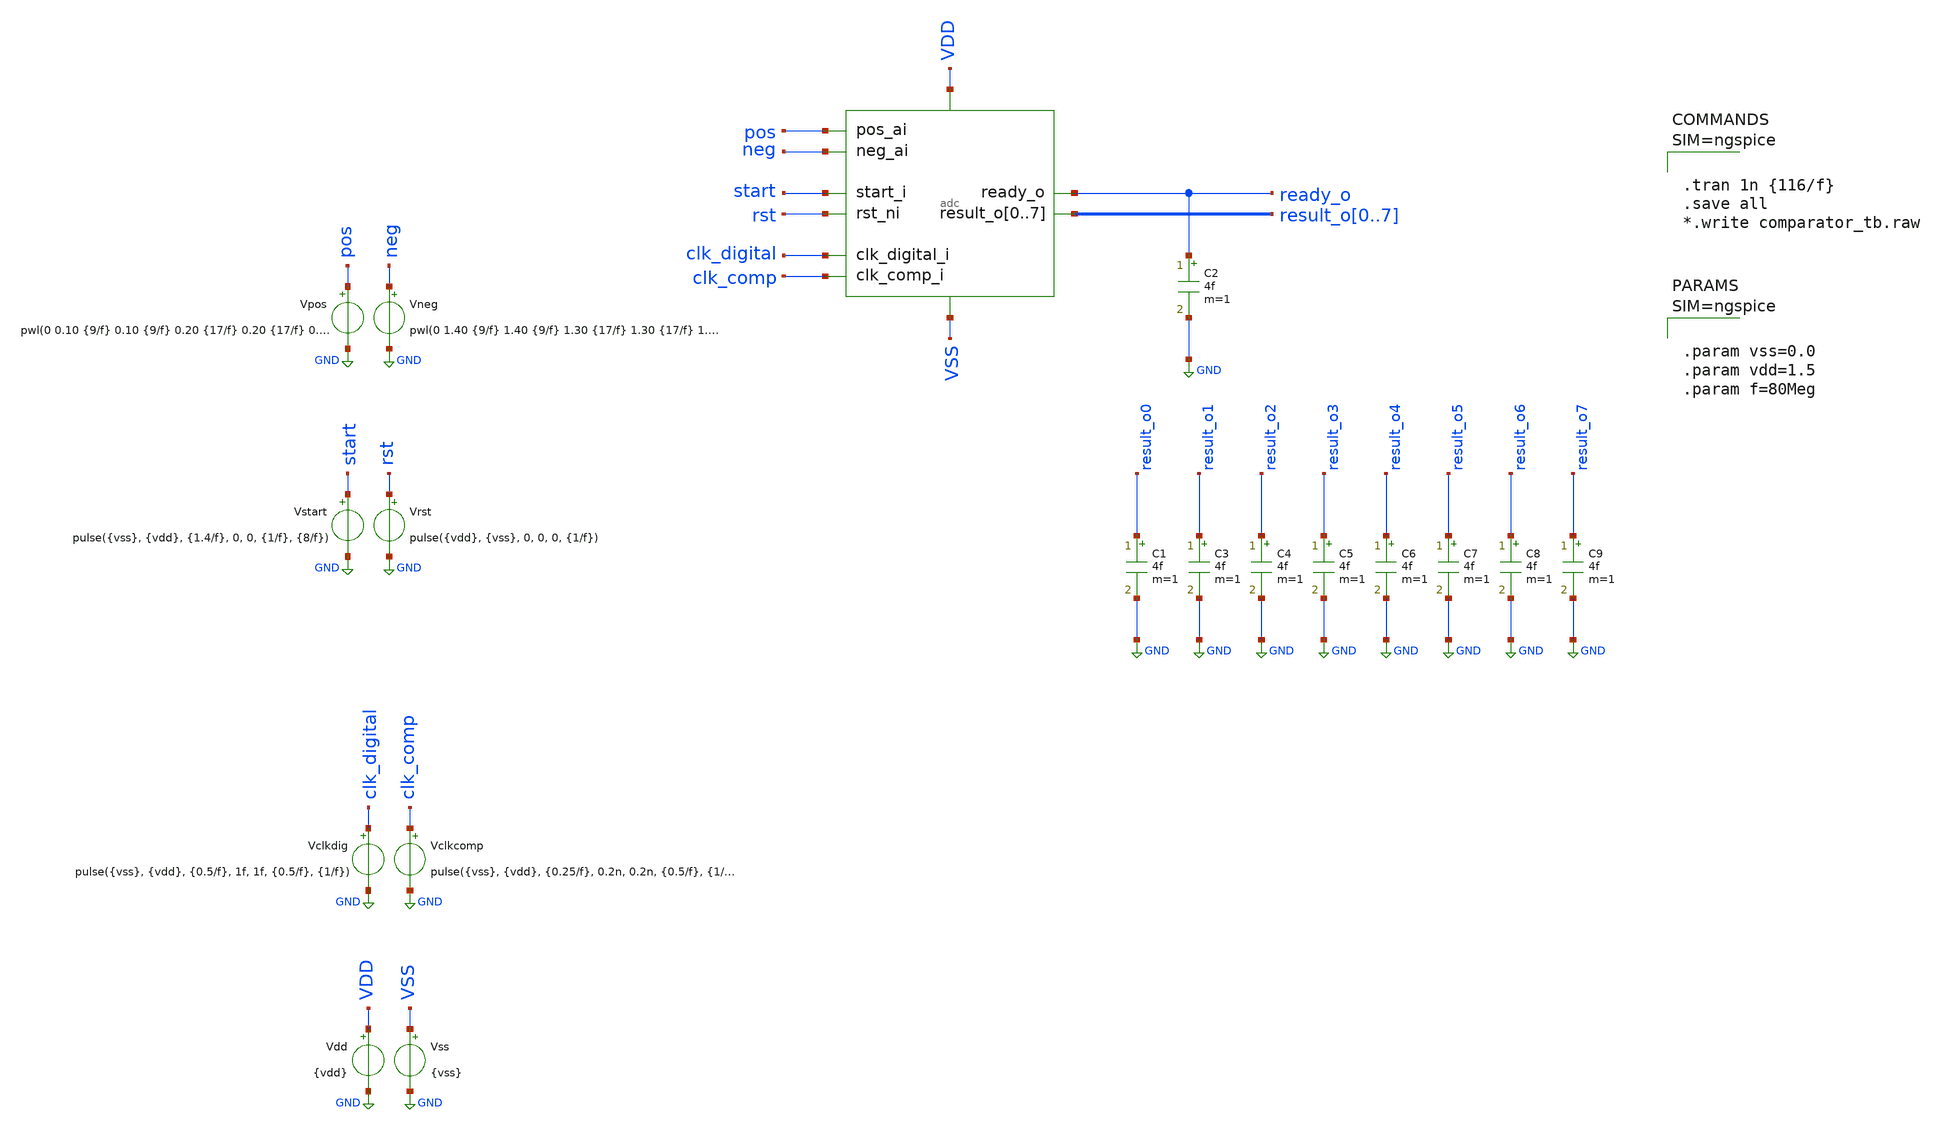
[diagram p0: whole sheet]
** sch_path: designs/diff/xschem/adc_tb.sch
* IHP-GmbH/IHP-Open-PDK/ihp-sg13g2/libs.tech/xschem/sg13g2_stdcells/sg13g2_inv_2.sch:
* Copyright 2023 IHP PDK Authors
* Licensed under the Apache License, Version 2.0 (the "License");
**.subckt adc_tb
x1 pos start rst clk_digital result_o0 result_o1 result_o2 result_o3 result_o4 result_o5 result_o6
+ result_o7 ready_o VDD VSS clk_comp neg adc
Vclkdig clk_digital GND pulse({vss}, {vdd}, {0.5/f}, 1f, 1f, {0.5/f}, {1/f})
Vrst rst GND pulse({vdd}, {vss}, 0, 0, 0, {1/f})
Vstart start GND pulse({vss}, {vdd}, {1.4/f}, 0, 0, {1/f}, {8/f})
Vpos pos GND pwl(0 0.10 {9/f} 0.10 {9/f} 0.20 {17/f} 0.20 {17/f} 0.30 {25/f} 0.30 {25/f} 0.40 {33/f}
+ 0.40 {33/f} 0.50 {41/f} 0.50 {41/f} 0.60 {49/f} 0.60 {49/f} 0.70 {57/f} 0.70 {57/f} 0.80 {65/f} 0.80
+ {65/f} 0.90 {73/f} 0.90 {73/f} 1.00 {81/f} 1.00 {81/f} 1.10 {89/f} 1.10 {89/f} 1.20 {97/f} 1.20 {97/f}
+ 1.30 {105/f} 1.30 {105/f} 1.40 {113/f} 1.40)
.save i(vpos)
Vdd VDD GND {vdd}
Vss VSS GND {vss}
C1 result_o0 GND 4f m=1
C2 ready_o GND 4f m=1
C3 result_o1 GND 4f m=1
C4 result_o2 GND 4f m=1
C5 result_o3 GND 4f m=1
Vclkcomp clk_comp GND pulse({vss}, {vdd}, {0.25/f}, 0.2n, 0.2n, {0.5/f}, {1/f})
C6 result_o4 GND 4f m=1
C7 result_o5 GND 4f m=1
C8 result_o6 GND 4f m=1
C9 result_o7 GND 4f m=1
Vneg neg GND pwl(0 1.40 {9/f} 1.40 {9/f} 1.30 {17/f} 1.30 {17/f} 1.20 {25/f} 1.20 {25/f} 1.10 {33/f}
+ 1.10 {33/f} 1.00 {41/f} 1.00 {41/f} 0.90 {49/f} 0.90 {49/f} 0.80 {57/f} 0.80 {57/f} 0.70 {65/f} 0.70
+ {65/f} 0.60 {73/f} 0.60 {73/f} 0.50 {81/f} 0.50 {81/f} 0.40 {89/f} 0.40 {89/f} 0.30 {97/f} 0.30 {97/f}
+ 0.20 {105/f} 0.20 {105/f} 0.10 {113/f} 0.10)
.save i(vneg)
**** begin user architecture code

.lib $::SG13G2_MODELS/cornerMOSlv.lib mos_tt
.lib $::SG13G2_MODELS/cornerCAP.lib cap_typ
.include $::PDK_ROOT/ihp-sg13g2/libs.ref/sg13g2_stdcell/spice/sg13g2_stdcell.spice




.tran 1n {116/f}
.save all
*.write comparator_tb.raw






.param vss=0.0
.param vdd=1.5
.param f=80Meg






.control
pre_set auto_bridge_d_out =  ( ".model auto_bridge_out bidi_bridge(direction=0 out_high=1.5
+ t_rise=0.2n t_fall=0.2n)"    "auto_bridge_out%d [ %s ] [ %s ] null auto_bridge_out" )
pre_set auto_bridge_d_in =  ( ".model auto_bridge_in bidi_bridge(direction=1 in_low=0.5 in_high=1)"
+    "auto_bridge_in%d [ %s ] [ %s ] null auto_bridge_in" )
.endc



**** end user architecture code
**.ends

* expanding   symbol:  adc.sym # of pins=10
** sym_path: designs/diff/xschem/adc.sym
** sch_path: designs/diff/xschem/adc.sch
.subckt adc pos_ai start_i rst_ni clk_digital_i result_o0 result_o1 result_o2 result_o3 result_o4
+ result_o5 result_o6 result_o7 ready_o VDD VSS clk_comp_i neg_ai
*.ipin pos_ai
*.ipin clk_digital_i
*.ipin VSS
*.ipin VDD
*.ipin rst_ni
*.ipin start_i
*.opin ready_o
*.opin result_o0,result_o1,result_o2,result_o3,result_o4,result_o5,result_o6,result_o7
*.ipin clk_comp_i
*.ipin neg_ai
A2 [ clk_digital_i ] [ net1 ] adc_buff_clk
A1 [ net1 start_i rst_ni comp_p comp_n ] [ sample dac_p0 dac_p1 dac_p2 dac_p3 dac_p4 dac_p5 dac_p6
+ dac_p7 dac_n0 dac_n1 dac_n2 dac_n3 dac_n4 dac_n5 dac_n6 dac_n7 ready_o result_o0 result_o1 result_o2
+ result_o3 result_o4 result_o5 result_o6 result_o7 ] adc
A3 [ %vd(pos neg) ] [ comp ] comp
A4 [ comp ] [ comp_a ] dac_buff
* noconn %vd(pos neg)
x2 net2 pos neg comp_2 comp_1 VSS VDD net3 comparator
x4 pos neg VSS VDD dac_p0 dac_p1 dac_p2 dac_p3 dac_p4 dac_p5 dac_p6 dac_p7 dac_n0 dac_n1 dac_n2
+ dac_n3 dac_n4 dac_n5 dac_n6 dac_n7 cdac
* noconn comp_a
XM5 comp_p comp_1 VSS VSS sg13_lv_nmos w=1.5u l=0.13u ng=1 m=1 mm_ok=1
XM6 comp_p comp_1 VDD VDD sg13_lv_pmos w=0.15u l=0.13u ng=1 m=1 mm_ok=1
XM7 comp_n comp_2 VSS VSS sg13_lv_nmos w=1.5u l=0.13u ng=1 m=1 mm_ok=1
XM8 comp_n comp_2 VDD VDD sg13_lv_pmos w=0.15u l=0.13u ng=1 m=1 mm_ok=1
.ends


* expanding   symbol:  ../../comparator/comparator.sym # of pins=8
** sym_path: designs/comparator_dt/comparator.sym
** sch_path: designs/comparator_dt/comparator.sch
.subckt comparator clk_i pos_ai neg_ai neg_o pos_o VSS VDD clk_ni
*.ipin pos_ai
*.ipin neg_ai
*.ipin VSS
*.ipin VDD
*.opin neg_o
*.opin pos_o
*.ipin clk_i
*.ipin clk_ni
XM12 neg_buf clk_i VDD VDD sg13_lv_pmos w=1.0u l=0.13u ng=1 m=1 mm_ok=1
XM13 pos_buf clk_i VDD VDD sg13_lv_pmos w=1.0u l=0.13u ng=1 m=1 mm_ok=1
XM14 net1 pos_ai neg_buf VSS sg13_lv_nmos w=1.0u l=0.13u ng=1 m=1 mm_ok=1
XM15 net1 neg_ai pos_buf VSS sg13_lv_nmos w=1.0u l=0.13u ng=1 m=1 mm_ok=1
XM16 VSS clk_i net1 VSS sg13_lv_nmos w=1.0u l=0.13u ng=1 m=1 mm_ok=1
XM17 net2 clk_ni VDD VDD sg13_lv_pmos w=2.0u l=0.13u ng=2 m=1 mm_ok=1
XM18 pos_o neg_o net2 VDD sg13_lv_pmos w=2.0u l=0.13u ng=2 m=1 mm_ok=1
XM19 neg_o pos_o net2 VDD sg13_lv_pmos w=2.0u l=0.13u ng=2 m=1 mm_ok=1
XM20 VSS neg_buf pos_o VSS sg13_lv_nmos w=1.0u l=0.13u ng=1 m=1 mm_ok=1
XM21 VSS neg_o pos_o VSS sg13_lv_nmos w=1.0u l=0.13u ng=1 m=1 mm_ok=1
XM22 VSS pos_o neg_o VSS sg13_lv_nmos w=1.0u l=0.13u ng=1 m=1 mm_ok=1
XM23 VSS pos_buf neg_o VSS sg13_lv_nmos w=1.0u l=0.13u ng=1 m=1 mm_ok=1
XC1 neg_buf VSS cap_cmim w=1.41e-5 l=1.41e-5 m=1 mm_ok=1
XC2 pos_buf VSS cap_cmim w=1.41e-5 l=1.41e-5 m=1 mm_ok=1
.ends


* expanding   symbol:  ../../cdac_diff/cdac.sym # of pins=6
** sym_path: designs/cdac_diff/cdac.sym
** sch_path: designs/cdac_diff/cdac.sch
.subckt cdac pos_ai neg_ai VSS VDD pos_ctrl_i0 pos_ctrl_i1 pos_ctrl_i2 pos_ctrl_i3 pos_ctrl_i4
+ pos_ctrl_i5 pos_ctrl_i6 pos_ctrl_i7 neg_ctrl_i0 neg_ctrl_i1 neg_ctrl_i2 neg_ctrl_i3 neg_ctrl_i4 neg_ctrl_i5
+ neg_ctrl_i6 neg_ctrl_i7
*.ipin pos_ai
*.ipin VSS
*.ipin VDD
*.ipin neg_ai
*.ipin
*+ pos_ctrl_i0,pos_ctrl_i1,pos_ctrl_i2,pos_ctrl_i3,pos_ctrl_i4,pos_ctrl_i5,pos_ctrl_i6,pos_ctrl_i7
*.ipin
*+ neg_ctrl_i0,neg_ctrl_i1,neg_ctrl_i2,neg_ctrl_i3,neg_ctrl_i4,neg_ctrl_i5,neg_ctrl_i6,neg_ctrl_i7
x1 net1 pos_ctrl_i0 VDD VSS sg13g2_inv_2
x2 net2 pos_ctrl_i1 VDD VSS sg13g2_inv_2
x3 net3 pos_ctrl_i2 VDD VSS sg13g2_inv_2
x4 net4 pos_ctrl_i3 VDD VSS sg13g2_inv_2
x5 net5 pos_ctrl_i4 VDD VSS sg13g2_inv_2
x6 net6 pos_ctrl_i5 VDD VSS sg13g2_inv_2
x7 net7 pos_ctrl_i6 VDD VSS sg13g2_inv_2
x8 net8 pos_ctrl_i7 VDD VSS sg13g2_inv_2
XC1 pos_ai net8 cap_cmim w=2.5292e-6 l=2.5292e-6 m=1 mm_ok=1
XC2 pos_ai net7 cap_cmim w=2.5292e-6 l=2.5292e-6 m=2 mm_ok=1
XC3 pos_ai net6 cap_cmim w=2.5292e-6 l=2.5292e-6 m=4 mm_ok=1
XC4 pos_ai net5 cap_cmim w=2.5292e-6 l=2.5292e-6 m=8 mm_ok=1
XC9 pos_ai VSS cap_cmim w=2.5292e-6 l=2.5292e-6 m=1 mm_ok=1
x9 net9 neg_ctrl_i0 VDD VSS sg13g2_inv_2
x10 net10 neg_ctrl_i1 VDD VSS sg13g2_inv_2
x11 net11 neg_ctrl_i2 VDD VSS sg13g2_inv_2
x12 net12 neg_ctrl_i3 VDD VSS sg13g2_inv_2
x13 net13 neg_ctrl_i4 VDD VSS sg13g2_inv_2
x14 net14 neg_ctrl_i5 VDD VSS sg13g2_inv_2
x15 net15 neg_ctrl_i6 VDD VSS sg13g2_inv_2
x16 net16 neg_ctrl_i7 VDD VSS sg13g2_inv_2
XC10 neg_ai net16 cap_cmim w=2.5292e-6 l=2.5292e-6 m=1 mm_ok=1
XC11 neg_ai net15 cap_cmim w=2.5292e-6 l=2.5292e-6 m=2 mm_ok=1
XC12 neg_ai net14 cap_cmim w=2.5292e-6 l=2.5292e-6 m=4 mm_ok=1
XC13 neg_ai net13 cap_cmim w=2.5292e-6 l=2.5292e-6 m=8 mm_ok=1
XC18 neg_ai VSS cap_cmim w=2.5292e-6 l=2.5292e-6 m=1 mm_ok=1
XC8 pos_ai net1 cap_cmim w=2.5292e-6 l=2.5292e-6 m=64 mm_ok=1
XC17 neg_ai net9 cap_cmim w=2.5292e-6 l=2.5292e-6 m=64 mm_ok=1
XC19 neg_ai net18 cap_cmim w=2.5292e-6 l=2.5292e-6 m=64 mm_ok=1
XC20 pos_ai net17 cap_cmim w=2.5292e-6 l=2.5292e-6 m=64 mm_ok=1
XC7 neg_ai net10 cap_cmim w=2.5292e-6 l=2.5292e-6 m=32 mm_ok=1
XC16 pos_ai net2 cap_cmim w=2.5292e-6 l=2.5292e-6 m=32 mm_ok=1
XC21 pos_ai net19 cap_cmim w=2.5292e-6 l=2.5292e-6 m=32 mm_ok=1
XC22 neg_ai net20 cap_cmim w=2.5292e-6 l=2.5292e-6 m=32 mm_ok=1
XC23 neg_ai net22 cap_cmim w=2.5292e-6 l=2.5292e-6 m=16 mm_ok=1
XC24 pos_ai net21 cap_cmim w=2.5292e-6 l=2.5292e-6 m=16 mm_ok=1
XC6 neg_ai net11 cap_cmim w=2.5292e-6 l=2.5292e-6 m=16 mm_ok=1
XC15 pos_ai net3 cap_cmim w=2.5292e-6 l=2.5292e-6 m=16 mm_ok=1
XC25 neg_ai net24 cap_cmim w=2.5292e-6 l=2.5292e-6 m=8 mm_ok=1
XC26 pos_ai net23 cap_cmim w=2.5292e-6 l=2.5292e-6 m=8 mm_ok=1
XC5 pos_ai net4 cap_cmim w=2.5292e-6 l=2.5292e-6 m=8 mm_ok=1
XC14 neg_ai net12 cap_cmim w=2.5292e-6 l=2.5292e-6 m=8 mm_ok=1
* noconn VDD
x17 net17 neg_ctrl_i0 VDD VSS sg13g2_buf_2
x21 net18 pos_ctrl_i0 VDD VSS sg13g2_buf_2
x18 net19 neg_ctrl_i1 VDD VSS sg13g2_buf_2
x19 net20 pos_ctrl_i1 VDD VSS sg13g2_buf_2
x20 net21 neg_ctrl_i2 VDD VSS sg13g2_buf_2
x22 net22 pos_ctrl_i2 VDD VSS sg13g2_buf_2
x23 net23 neg_ctrl_i3 VDD VSS sg13g2_buf_2
x24 net24 pos_ctrl_i3 VDD VSS sg13g2_buf_2
.ends


* expanding   symbol:  sg13g2_stdcells/sg13g2_inv_2.sym # of pins=2
** sym_path: sg13g2_stdcells/sg13g2_inv_2.sym
** sch_path: sg13g2_stdcells/sg13g2_inv_2.sch
.subckt sg13g2_inv_2 Y A VDD VSS
*.opin Y
*.ipin A
*.iopin VDD
*.iopin VSS
XM1 Y A VSS VSS sg13_lv_nmos w=1.48u l=130.00n ng=2 m=1 mm_ok=1
XM2 Y A VDD VDD sg13_lv_pmos w=2.24u l=130.00n ng=2 m=1 mm_ok=1
.ends


* expanding   symbol:  sg13g2_stdcells/sg13g2_buf_2.sym # of pins=2
** sym_path: sg13g2_stdcells/sg13g2_buf_2.sym
** sch_path: sg13g2_stdcells/sg13g2_buf_2.sch
.subckt sg13g2_buf_2 X A VDD VSS
*.ipin A
*.opin X
*.iopin VDD
*.iopin VSS
XM1 net1 A VSS VSS sg13_lv_nmos w=640.00n l=130.00n ng=1 m=1 mm_ok=1
XM2 X net1 VSS VSS sg13_lv_nmos w=1.48u l=130.00n ng=2 m=1 mm_ok=1
XM3 net1 A VDD VDD sg13_lv_pmos w=1.000u l=130.00n ng=1 m=1 mm_ok=1
XM4 X net1 VDD VDD sg13_lv_pmos w=2.24u l=130.00n ng=2 m=1 mm_ok=1
.ends

.GLOBAL GND
**** begin user architecture code
.model adc d_cosim simulation="ivlng" sim_args=["adc"]
.model dac_buff dac_bridge input_load=1e-15 t_rise=0.1n t_fall=0.1n  out_low=0 out_high=1.5
.model comp adc_bridge in_low=0 in_high=0
**** end user architecture code
.end
